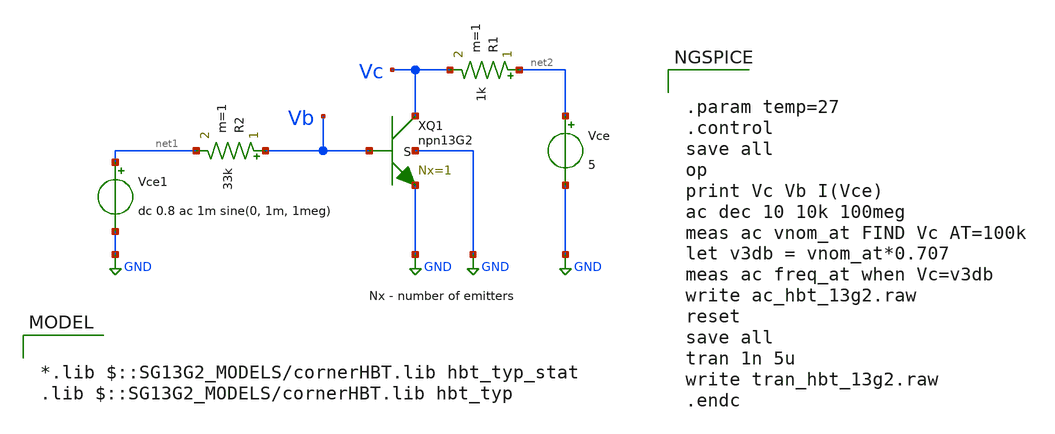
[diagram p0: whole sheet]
** sch_path: ihp-sg13g2/libs.tech/xschem/sg13g2_tests/tran_hbt_13g2.sch
* Copyright 2023 IHP PDK Authors
**.subckt tran_hbt_13g2
Vce net2 GND 5
XQ1 Vc Vb GND GND npn13G2 Nx=1
R1 net2 Vc 1k m=1
Vce1 net1 GND dc 0.8 ac 1m sine(0, 1m, 1meg)
R2 Vb net1 33k m=1
**** begin user architecture code

*.lib $::SG13G2_MODELS/cornerHBT.lib hbt_typ_stat
.lib $::SG13G2_MODELS/cornerHBT.lib hbt_typ



.param temp=27
.control
save all
op
print Vc Vb I(Vce)
ac dec 10 10k 100meg
meas ac vnom_at FIND Vc AT=100k
let v3db = vnom_at*0.707
meas ac freq_at when Vc=v3db
write ac_hbt_13g2.raw
reset
save all
tran 1n 5u
write tran_hbt_13g2.raw
.endc


**** end user architecture code
**.ends
.GLOBAL GND
.end
